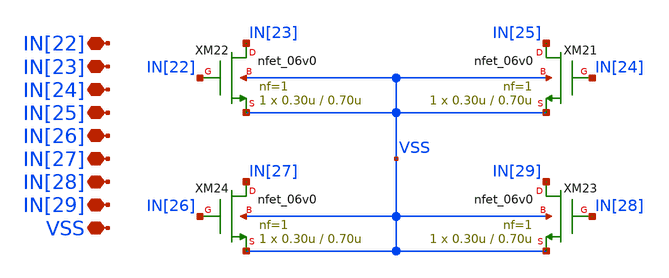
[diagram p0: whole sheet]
** sch_path: designs/libs/core_single-fet/nfet-com/nfet-com.sch
**.subckt nfet-com IN[22] IN[23] IN[24] IN[25] IN[26] IN[27] IN[28] IN[29] VSS
*.iopin IN[22]
*.iopin IN[23]
*.iopin IN[24]
*.iopin IN[25]
*.iopin IN[26]
*.iopin IN[27]
*.iopin IN[28]
*.iopin IN[29]
*.iopin VSS
XM21 IN[25] IN[24] VSS VSS nfet_06v0 L=0.70u W=0.30u nf=1 ad='int((nf+1)/2) * W/nf * 0.18u' as='int((nf+2)/2) * W/nf * 0.18u'
+ pd='2*int((nf+1)/2) * (W/nf + 0.18u)' ps='2*int((nf+2)/2) * (W/nf + 0.18u)' nrd='0.18u / W' nrs='0.18u / W'
+ sa=0 sb=0 sd=0 m=1
XM22 IN[23] IN[22] VSS VSS nfet_06v0 L=0.70u W=0.30u nf=1 ad='int((nf+1)/2) * W/nf * 0.18u' as='int((nf+2)/2) * W/nf * 0.18u'
+ pd='2*int((nf+1)/2) * (W/nf + 0.18u)' ps='2*int((nf+2)/2) * (W/nf + 0.18u)' nrd='0.18u / W' nrs='0.18u / W'
+ sa=0 sb=0 sd=0 m=1
XM23 IN[29] IN[28] VSS VSS nfet_06v0 L=0.70u W=0.30u nf=1 ad='int((nf+1)/2) * W/nf * 0.18u' as='int((nf+2)/2) * W/nf * 0.18u'
+ pd='2*int((nf+1)/2) * (W/nf + 0.18u)' ps='2*int((nf+2)/2) * (W/nf + 0.18u)' nrd='0.18u / W' nrs='0.18u / W'
+ sa=0 sb=0 sd=0 m=1
XM24 IN[27] IN[26] VSS VSS nfet_06v0 L=0.70u W=0.30u nf=1 ad='int((nf+1)/2) * W/nf * 0.18u' as='int((nf+2)/2) * W/nf * 0.18u'
+ pd='2*int((nf+1)/2) * (W/nf + 0.18u)' ps='2*int((nf+2)/2) * (W/nf + 0.18u)' nrd='0.18u / W' nrs='0.18u / W'
+ sa=0 sb=0 sd=0 m=1
**.ends
.end
